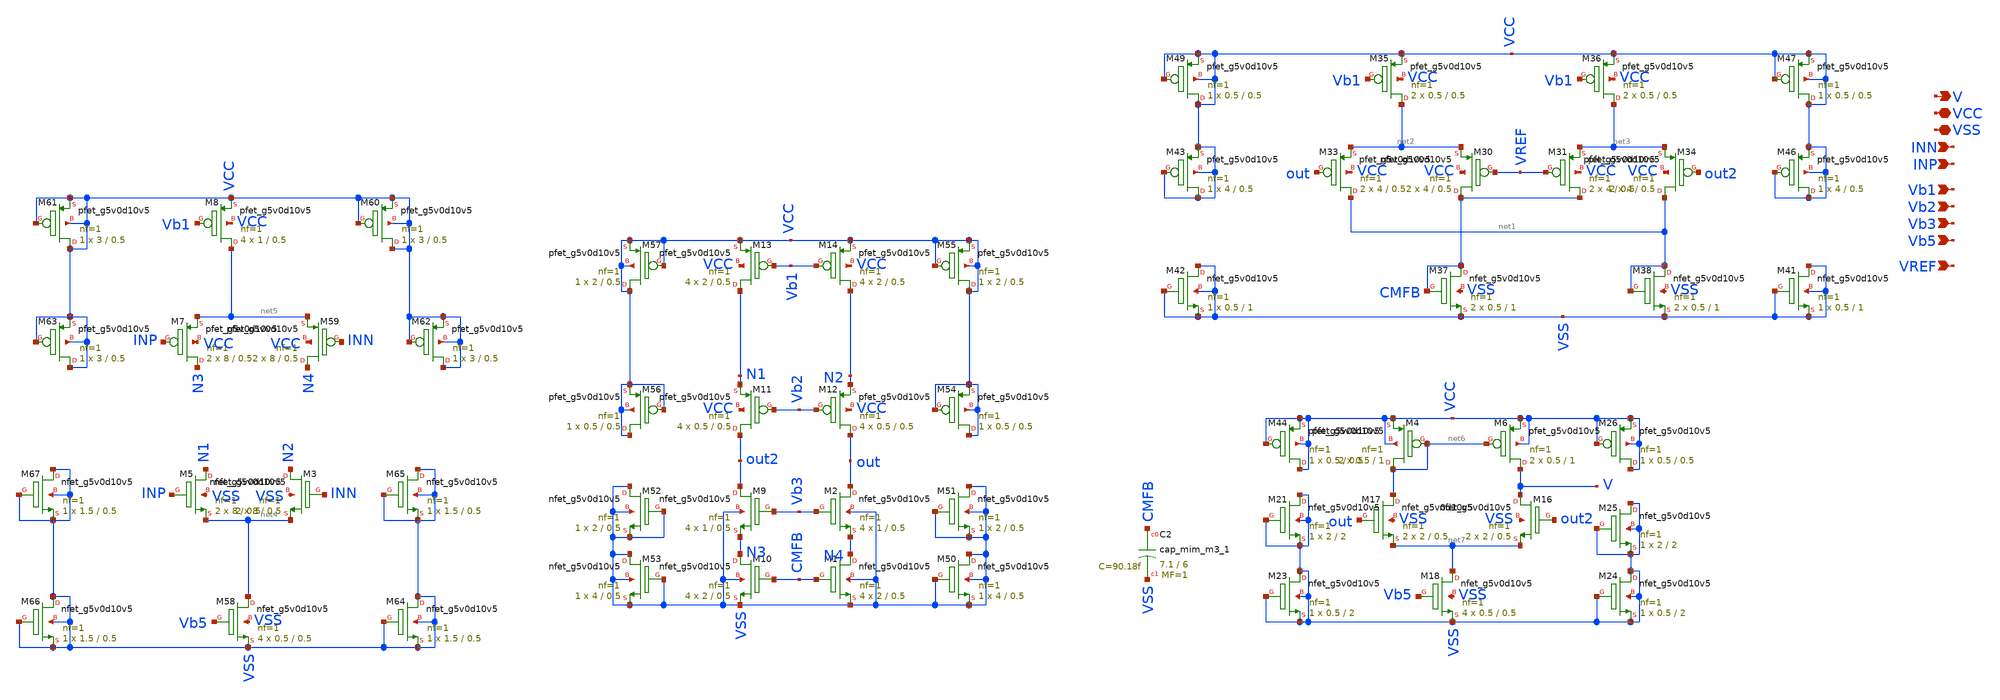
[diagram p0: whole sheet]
** sch_path: latest_working_comparator/total.sch
**.subckt total V VCC VSS INN INP Vb1 Vb2 Vb3 Vb5 VREF
*.opin V
*.iopin VCC
*.iopin VSS
*.ipin INN
*.ipin INP
*.ipin Vb1
*.ipin Vb2
*.ipin Vb3
*.ipin Vb5
*.ipin VREF
XM1 N4 CMFB VSS VSS sky130_fd_pr__nfet_g5v0d10v5 L=0.5 W=2 nf=1 ad='int((nf+1)/2) * W/nf * 0.29' as='int((nf+2)/2) * W/nf * 0.29'
+ pd='2*int((nf+1)/2) * (W/nf + 0.29)' ps='2*int((nf+2)/2) * (W/nf + 0.29)' nrd='0.29 / W' nrs='0.29 / W'
+ sa=0 sb=0 sd=0 mult=4 m=4
XM2 out Vb3 N4 VSS sky130_fd_pr__nfet_g5v0d10v5 L=0.5 W=1 nf=1 ad='int((nf+1)/2) * W/nf * 0.29' as='int((nf+2)/2) * W/nf * 0.29'
+ pd='2*int((nf+1)/2) * (W/nf + 0.29)' ps='2*int((nf+2)/2) * (W/nf + 0.29)' nrd='0.29 / W' nrs='0.29 / W'
+ sa=0 sb=0 sd=0 mult=4 m=4
XM9 out2 Vb3 N3 VSS sky130_fd_pr__nfet_g5v0d10v5 L=0.5 W=1 nf=1 ad='int((nf+1)/2) * W/nf * 0.29' as='int((nf+2)/2) * W/nf * 0.29'
+ pd='2*int((nf+1)/2) * (W/nf + 0.29)' ps='2*int((nf+2)/2) * (W/nf + 0.29)' nrd='0.29 / W' nrs='0.29 / W'
+ sa=0 sb=0 sd=0 mult=4 m=4
XM10 N3 CMFB VSS VSS sky130_fd_pr__nfet_g5v0d10v5 L=0.5 W=2 nf=1 ad='int((nf+1)/2) * W/nf * 0.29' as='int((nf+2)/2) * W/nf * 0.29'
+ pd='2*int((nf+1)/2) * (W/nf + 0.29)' ps='2*int((nf+2)/2) * (W/nf + 0.29)' nrd='0.29 / W' nrs='0.29 / W'
+ sa=0 sb=0 sd=0 mult=4 m=4
XM11 out2 Vb2 N1 VCC sky130_fd_pr__pfet_g5v0d10v5 L=0.5 W=0.5 nf=1 ad='int((nf+1)/2) * W/nf * 0.29' as='int((nf+2)/2) * W/nf * 0.29'
+ pd='2*int((nf+1)/2) * (W/nf + 0.29)' ps='2*int((nf+2)/2) * (W/nf + 0.29)' nrd='0.29 / W' nrs='0.29 / W'
+ sa=0 sb=0 sd=0 mult=4 m=4
XM12 out Vb2 N2 VCC sky130_fd_pr__pfet_g5v0d10v5 L=0.5 W=0.5 nf=1 ad='int((nf+1)/2) * W/nf * 0.29' as='int((nf+2)/2) * W/nf * 0.29'
+ pd='2*int((nf+1)/2) * (W/nf + 0.29)' ps='2*int((nf+2)/2) * (W/nf + 0.29)' nrd='0.29 / W' nrs='0.29 / W'
+ sa=0 sb=0 sd=0 mult=4 m=4
XM13 N1 Vb1 VCC VCC sky130_fd_pr__pfet_g5v0d10v5 L=0.5 W=2 nf=1 ad='int((nf+1)/2) * W/nf * 0.29' as='int((nf+2)/2) * W/nf * 0.29'
+ pd='2*int((nf+1)/2) * (W/nf + 0.29)' ps='2*int((nf+2)/2) * (W/nf + 0.29)' nrd='0.29 / W' nrs='0.29 / W'
+ sa=0 sb=0 sd=0 mult=4 m=4
XM14 N2 Vb1 VCC VCC sky130_fd_pr__pfet_g5v0d10v5 L=0.5 W=2 nf=1 ad='int((nf+1)/2) * W/nf * 0.29' as='int((nf+2)/2) * W/nf * 0.29'
+ pd='2*int((nf+1)/2) * (W/nf + 0.29)' ps='2*int((nf+2)/2) * (W/nf + 0.29)' nrd='0.29 / W' nrs='0.29 / W'
+ sa=0 sb=0 sd=0 mult=4 m=4
XM30 CMFB VREF net2 VCC sky130_fd_pr__pfet_g5v0d10v5 L=0.5 W=4 nf=1 ad='int((nf+1)/2) * W/nf * 0.29'
+ as='int((nf+2)/2) * W/nf * 0.29' pd='2*int((nf+1)/2) * (W/nf + 0.29)' ps='2*int((nf+2)/2) * (W/nf + 0.29)'
+ nrd='0.29 / W' nrs='0.29 / W' sa=0 sb=0 sd=0 mult=2 m=2
XM31 CMFB VREF net3 VCC sky130_fd_pr__pfet_g5v0d10v5 L=0.5 W=4 nf=1 ad='int((nf+1)/2) * W/nf * 0.29'
+ as='int((nf+2)/2) * W/nf * 0.29' pd='2*int((nf+1)/2) * (W/nf + 0.29)' ps='2*int((nf+2)/2) * (W/nf + 0.29)'
+ nrd='0.29 / W' nrs='0.29 / W' sa=0 sb=0 sd=0 mult=2 m=2
XM33 net1 out net2 VCC sky130_fd_pr__pfet_g5v0d10v5 L=0.5 W=4 nf=1 ad='int((nf+1)/2) * W/nf * 0.29' as='int((nf+2)/2) * W/nf * 0.29'
+ pd='2*int((nf+1)/2) * (W/nf + 0.29)' ps='2*int((nf+2)/2) * (W/nf + 0.29)' nrd='0.29 / W' nrs='0.29 / W'
+ sa=0 sb=0 sd=0 mult=2 m=2
XM34 net1 out2 net3 VCC sky130_fd_pr__pfet_g5v0d10v5 L=0.5 W=4 nf=1 ad='int((nf+1)/2) * W/nf * 0.29'
+ as='int((nf+2)/2) * W/nf * 0.29' pd='2*int((nf+1)/2) * (W/nf + 0.29)' ps='2*int((nf+2)/2) * (W/nf + 0.29)'
+ nrd='0.29 / W' nrs='0.29 / W' sa=0 sb=0 sd=0 mult=2 m=2
XM35 net2 Vb1 VCC VCC sky130_fd_pr__pfet_g5v0d10v5 L=0.5 W=0.5 nf=1 ad='int((nf+1)/2) * W/nf * 0.29'
+ as='int((nf+2)/2) * W/nf * 0.29' pd='2*int((nf+1)/2) * (W/nf + 0.29)' ps='2*int((nf+2)/2) * (W/nf + 0.29)'
+ nrd='0.29 / W' nrs='0.29 / W' sa=0 sb=0 sd=0 mult=2 m=2
XM36 net3 Vb1 VCC VCC sky130_fd_pr__pfet_g5v0d10v5 L=0.5 W=0.5 nf=1 ad='int((nf+1)/2) * W/nf * 0.29'
+ as='int((nf+2)/2) * W/nf * 0.29' pd='2*int((nf+1)/2) * (W/nf + 0.29)' ps='2*int((nf+2)/2) * (W/nf + 0.29)'
+ nrd='0.29 / W' nrs='0.29 / W' sa=0 sb=0 sd=0 mult=2 m=2
XM37 CMFB CMFB VSS VSS sky130_fd_pr__nfet_g5v0d10v5 L=1 W=0.5 nf=1 ad='int((nf+1)/2) * W/nf * 0.29' as='int((nf+2)/2) * W/nf * 0.29'
+ pd='2*int((nf+1)/2) * (W/nf + 0.29)' ps='2*int((nf+2)/2) * (W/nf + 0.29)' nrd='0.29 / W' nrs='0.29 / W'
+ sa=0 sb=0 sd=0 mult=2 m=2
XM38 net1 net1 VSS VSS sky130_fd_pr__nfet_g5v0d10v5 L=1 W=0.5 nf=1 ad='int((nf+1)/2) * W/nf * 0.29' as='int((nf+2)/2) * W/nf * 0.29'
+ pd='2*int((nf+1)/2) * (W/nf + 0.29)' ps='2*int((nf+2)/2) * (W/nf + 0.29)' nrd='0.29 / W' nrs='0.29 / W'
+ sa=0 sb=0 sd=0 mult=2 m=2
XM41 VSS VSS VSS VSS sky130_fd_pr__nfet_g5v0d10v5 L=1 W=0.5 nf=1 ad='int((nf+1)/2) * W/nf * 0.29' as='int((nf+2)/2) * W/nf * 0.29'
+ pd='2*int((nf+1)/2) * (W/nf + 0.29)' ps='2*int((nf+2)/2) * (W/nf + 0.29)' nrd='0.29 / W' nrs='0.29 / W'
+ sa=0 sb=0 sd=0 mult=1 m=1
XM42 VSS VSS VSS VSS sky130_fd_pr__nfet_g5v0d10v5 L=1 W=0.5 nf=1 ad='int((nf+1)/2) * W/nf * 0.29' as='int((nf+2)/2) * W/nf * 0.29'
+ pd='2*int((nf+1)/2) * (W/nf + 0.29)' ps='2*int((nf+2)/2) * (W/nf + 0.29)' nrd='0.29 / W' nrs='0.29 / W'
+ sa=0 sb=0 sd=0 mult=1 m=1
XM43 VCC VCC VCC VCC sky130_fd_pr__pfet_g5v0d10v5 L=0.5 W=4 nf=1 ad='int((nf+1)/2) * W/nf * 0.29' as='int((nf+2)/2) * W/nf * 0.29'
+ pd='2*int((nf+1)/2) * (W/nf + 0.29)' ps='2*int((nf+2)/2) * (W/nf + 0.29)' nrd='0.29 / W' nrs='0.29 / W'
+ sa=0 sb=0 sd=0 mult=1 m=1
XM47 VCC VCC VCC VCC sky130_fd_pr__pfet_g5v0d10v5 L=0.5 W=0.5 nf=1 ad='int((nf+1)/2) * W/nf * 0.29' as='int((nf+2)/2) * W/nf * 0.29'
+ pd='2*int((nf+1)/2) * (W/nf + 0.29)' ps='2*int((nf+2)/2) * (W/nf + 0.29)' nrd='0.29 / W' nrs='0.29 / W'
+ sa=0 sb=0 sd=0 mult=1 m=1
XM49 VCC VCC VCC VCC sky130_fd_pr__pfet_g5v0d10v5 L=0.5 W=0.5 nf=1 ad='int((nf+1)/2) * W/nf * 0.29' as='int((nf+2)/2) * W/nf * 0.29'
+ pd='2*int((nf+1)/2) * (W/nf + 0.29)' ps='2*int((nf+2)/2) * (W/nf + 0.29)' nrd='0.29 / W' nrs='0.29 / W'
+ sa=0 sb=0 sd=0 mult=1 m=1
XM46 VCC VCC VCC VCC sky130_fd_pr__pfet_g5v0d10v5 L=0.5 W=4 nf=1 ad='int((nf+1)/2) * W/nf * 0.29' as='int((nf+2)/2) * W/nf * 0.29'
+ pd='2*int((nf+1)/2) * (W/nf + 0.29)' ps='2*int((nf+2)/2) * (W/nf + 0.29)' nrd='0.29 / W' nrs='0.29 / W'
+ sa=0 sb=0 sd=0 mult=1 m=1
XM50 VSS VSS VSS VSS sky130_fd_pr__nfet_g5v0d10v5 L=0.5 W=4 nf=1 ad='int((nf+1)/2) * W/nf * 0.29' as='int((nf+2)/2) * W/nf * 0.29'
+ pd='2*int((nf+1)/2) * (W/nf + 0.29)' ps='2*int((nf+2)/2) * (W/nf + 0.29)' nrd='0.29 / W' nrs='0.29 / W'
+ sa=0 sb=0 sd=0 mult=1 m=1
XM51 VSS VSS VSS VSS sky130_fd_pr__nfet_g5v0d10v5 L=0.5 W=2 nf=1 ad='int((nf+1)/2) * W/nf * 0.29' as='int((nf+2)/2) * W/nf * 0.29'
+ pd='2*int((nf+1)/2) * (W/nf + 0.29)' ps='2*int((nf+2)/2) * (W/nf + 0.29)' nrd='0.29 / W' nrs='0.29 / W'
+ sa=0 sb=0 sd=0 mult=1 m=1
XM52 VSS VSS VSS VSS sky130_fd_pr__nfet_g5v0d10v5 L=0.5 W=2 nf=1 ad='int((nf+1)/2) * W/nf * 0.29' as='int((nf+2)/2) * W/nf * 0.29'
+ pd='2*int((nf+1)/2) * (W/nf + 0.29)' ps='2*int((nf+2)/2) * (W/nf + 0.29)' nrd='0.29 / W' nrs='0.29 / W'
+ sa=0 sb=0 sd=0 mult=1 m=1
XM53 VSS VSS VSS VSS sky130_fd_pr__nfet_g5v0d10v5 L=0.5 W=4 nf=1 ad='int((nf+1)/2) * W/nf * 0.29' as='int((nf+2)/2) * W/nf * 0.29'
+ pd='2*int((nf+1)/2) * (W/nf + 0.29)' ps='2*int((nf+2)/2) * (W/nf + 0.29)' nrd='0.29 / W' nrs='0.29 / W'
+ sa=0 sb=0 sd=0 mult=1 m=1
XM54 VCC VCC VCC VCC sky130_fd_pr__pfet_g5v0d10v5 L=0.5 W=0.5 nf=1 ad='int((nf+1)/2) * W/nf * 0.29' as='int((nf+2)/2) * W/nf * 0.29'
+ pd='2*int((nf+1)/2) * (W/nf + 0.29)' ps='2*int((nf+2)/2) * (W/nf + 0.29)' nrd='0.29 / W' nrs='0.29 / W'
+ sa=0 sb=0 sd=0 mult=1 m=1
XM55 VCC VCC VCC VCC sky130_fd_pr__pfet_g5v0d10v5 L=0.5 W=2 nf=1 ad='int((nf+1)/2) * W/nf * 0.29' as='int((nf+2)/2) * W/nf * 0.29'
+ pd='2*int((nf+1)/2) * (W/nf + 0.29)' ps='2*int((nf+2)/2) * (W/nf + 0.29)' nrd='0.29 / W' nrs='0.29 / W'
+ sa=0 sb=0 sd=0 mult=1 m=1
XM56 VCC VCC VCC VCC sky130_fd_pr__pfet_g5v0d10v5 L=0.5 W=0.5 nf=1 ad='int((nf+1)/2) * W/nf * 0.29' as='int((nf+2)/2) * W/nf * 0.29'
+ pd='2*int((nf+1)/2) * (W/nf + 0.29)' ps='2*int((nf+2)/2) * (W/nf + 0.29)' nrd='0.29 / W' nrs='0.29 / W'
+ sa=0 sb=0 sd=0 mult=1 m=1
XM57 VCC VCC VCC VCC sky130_fd_pr__pfet_g5v0d10v5 L=0.5 W=2 nf=1 ad='int((nf+1)/2) * W/nf * 0.29' as='int((nf+2)/2) * W/nf * 0.29'
+ pd='2*int((nf+1)/2) * (W/nf + 0.29)' ps='2*int((nf+2)/2) * (W/nf + 0.29)' nrd='0.29 / W' nrs='0.29 / W'
+ sa=0 sb=0 sd=0 mult=1 m=1
XC2 CMFB VSS sky130_fd_pr__cap_mim_m3_1 W=7.1 L=6 MF=1 m=1
XM3 N2 INN net4 VSS sky130_fd_pr__nfet_g5v0d10v5 L=0.5 W=8 nf=1 ad='int((nf+1)/2) * W/nf * 0.29' as='int((nf+2)/2) * W/nf * 0.29'
+ pd='2*int((nf+1)/2) * (W/nf + 0.29)' ps='2*int((nf+2)/2) * (W/nf + 0.29)' nrd='0.29 / W' nrs='0.29 / W'
+ sa=0 sb=0 sd=0 mult=2 m=2
XM5 N1 INP net4 VSS sky130_fd_pr__nfet_g5v0d10v5 L=0.5 W=8 nf=1 ad='int((nf+1)/2) * W/nf * 0.29' as='int((nf+2)/2) * W/nf * 0.29'
+ pd='2*int((nf+1)/2) * (W/nf + 0.29)' ps='2*int((nf+2)/2) * (W/nf + 0.29)' nrd='0.29 / W' nrs='0.29 / W'
+ sa=0 sb=0 sd=0 mult=2 m=2
XM7 N3 INP net5 VCC sky130_fd_pr__pfet_g5v0d10v5 L=0.5 W=8 nf=1 ad='int((nf+1)/2) * W/nf * 0.29' as='int((nf+2)/2) * W/nf * 0.29'
+ pd='2*int((nf+1)/2) * (W/nf + 0.29)' ps='2*int((nf+2)/2) * (W/nf + 0.29)' nrd='0.29 / W' nrs='0.29 / W'
+ sa=0 sb=0 sd=0 mult=2 m=2
XM8 net5 Vb1 VCC VCC sky130_fd_pr__pfet_g5v0d10v5 L=0.5 W=1 nf=1 ad='int((nf+1)/2) * W/nf * 0.29' as='int((nf+2)/2) * W/nf * 0.29'
+ pd='2*int((nf+1)/2) * (W/nf + 0.29)' ps='2*int((nf+2)/2) * (W/nf + 0.29)' nrd='0.29 / W' nrs='0.29 / W'
+ sa=0 sb=0 sd=0 mult=4 m=4
XM58 net4 Vb5 VSS VSS sky130_fd_pr__nfet_g5v0d10v5 L=0.5 W=0.5 nf=1 ad='int((nf+1)/2) * W/nf * 0.29'
+ as='int((nf+2)/2) * W/nf * 0.29' pd='2*int((nf+1)/2) * (W/nf + 0.29)' ps='2*int((nf+2)/2) * (W/nf + 0.29)'
+ nrd='0.29 / W' nrs='0.29 / W' sa=0 sb=0 sd=0 mult=4 m=4
XM59 N4 INN net5 VCC sky130_fd_pr__pfet_g5v0d10v5 L=0.5 W=8 nf=1 ad='int((nf+1)/2) * W/nf * 0.29' as='int((nf+2)/2) * W/nf * 0.29'
+ pd='2*int((nf+1)/2) * (W/nf + 0.29)' ps='2*int((nf+2)/2) * (W/nf + 0.29)' nrd='0.29 / W' nrs='0.29 / W'
+ sa=0 sb=0 sd=0 mult=2 m=2
XM60 VCC VCC VCC VCC sky130_fd_pr__pfet_g5v0d10v5 L=0.5 W=3 nf=1 ad='int((nf+1)/2) * W/nf * 0.29' as='int((nf+2)/2) * W/nf * 0.29'
+ pd='2*int((nf+1)/2) * (W/nf + 0.29)' ps='2*int((nf+2)/2) * (W/nf + 0.29)' nrd='0.29 / W' nrs='0.29 / W'
+ sa=0 sb=0 sd=0 mult=1 m=1
XM61 VCC VCC VCC VCC sky130_fd_pr__pfet_g5v0d10v5 L=0.5 W=3 nf=1 ad='int((nf+1)/2) * W/nf * 0.29' as='int((nf+2)/2) * W/nf * 0.29'
+ pd='2*int((nf+1)/2) * (W/nf + 0.29)' ps='2*int((nf+2)/2) * (W/nf + 0.29)' nrd='0.29 / W' nrs='0.29 / W'
+ sa=0 sb=0 sd=0 mult=1 m=1
XM62 VCC VCC VCC VCC sky130_fd_pr__pfet_g5v0d10v5 L=0.5 W=3 nf=1 ad='int((nf+1)/2) * W/nf * 0.29' as='int((nf+2)/2) * W/nf * 0.29'
+ pd='2*int((nf+1)/2) * (W/nf + 0.29)' ps='2*int((nf+2)/2) * (W/nf + 0.29)' nrd='0.29 / W' nrs='0.29 / W'
+ sa=0 sb=0 sd=0 mult=1 m=1
XM63 VCC VCC VCC VCC sky130_fd_pr__pfet_g5v0d10v5 L=0.5 W=3 nf=1 ad='int((nf+1)/2) * W/nf * 0.29' as='int((nf+2)/2) * W/nf * 0.29'
+ pd='2*int((nf+1)/2) * (W/nf + 0.29)' ps='2*int((nf+2)/2) * (W/nf + 0.29)' nrd='0.29 / W' nrs='0.29 / W'
+ sa=0 sb=0 sd=0 mult=1 m=1
XM64 VSS VSS VSS VSS sky130_fd_pr__nfet_g5v0d10v5 L=0.5 W=1.5 nf=1 ad='int((nf+1)/2) * W/nf * 0.29' as='int((nf+2)/2) * W/nf * 0.29'
+ pd='2*int((nf+1)/2) * (W/nf + 0.29)' ps='2*int((nf+2)/2) * (W/nf + 0.29)' nrd='0.29 / W' nrs='0.29 / W'
+ sa=0 sb=0 sd=0 mult=1 m=1
XM65 VSS VSS VSS VSS sky130_fd_pr__nfet_g5v0d10v5 L=0.5 W=1.5 nf=1 ad='int((nf+1)/2) * W/nf * 0.29' as='int((nf+2)/2) * W/nf * 0.29'
+ pd='2*int((nf+1)/2) * (W/nf + 0.29)' ps='2*int((nf+2)/2) * (W/nf + 0.29)' nrd='0.29 / W' nrs='0.29 / W'
+ sa=0 sb=0 sd=0 mult=1 m=1
XM66 VSS VSS VSS VSS sky130_fd_pr__nfet_g5v0d10v5 L=0.5 W=1.5 nf=1 ad='int((nf+1)/2) * W/nf * 0.29' as='int((nf+2)/2) * W/nf * 0.29'
+ pd='2*int((nf+1)/2) * (W/nf + 0.29)' ps='2*int((nf+2)/2) * (W/nf + 0.29)' nrd='0.29 / W' nrs='0.29 / W'
+ sa=0 sb=0 sd=0 mult=1 m=1
XM67 VSS VSS VSS VSS sky130_fd_pr__nfet_g5v0d10v5 L=0.5 W=1.5 nf=1 ad='int((nf+1)/2) * W/nf * 0.29' as='int((nf+2)/2) * W/nf * 0.29'
+ pd='2*int((nf+1)/2) * (W/nf + 0.29)' ps='2*int((nf+2)/2) * (W/nf + 0.29)' nrd='0.29 / W' nrs='0.29 / W'
+ sa=0 sb=0 sd=0 mult=1 m=1
XM4 net6 net6 VCC VCC sky130_fd_pr__pfet_g5v0d10v5 L=1 W=0.5 nf=1 ad='int((nf+1)/2) * W/nf * 0.29' as='int((nf+2)/2) * W/nf * 0.29'
+ pd='2*int((nf+1)/2) * (W/nf + 0.29)' ps='2*int((nf+2)/2) * (W/nf + 0.29)' nrd='0.29 / W' nrs='0.29 / W'
+ sa=0 sb=0 sd=0 mult=2 m=2
XM6 V net6 VCC VCC sky130_fd_pr__pfet_g5v0d10v5 L=1 W=0.5 nf=1 ad='int((nf+1)/2) * W/nf * 0.29' as='int((nf+2)/2) * W/nf * 0.29'
+ pd='2*int((nf+1)/2) * (W/nf + 0.29)' ps='2*int((nf+2)/2) * (W/nf + 0.29)' nrd='0.29 / W' nrs='0.29 / W'
+ sa=0 sb=0 sd=0 mult=2 m=2
XM16 V out2 net7 VSS sky130_fd_pr__nfet_g5v0d10v5 L=0.5 W=2 nf=1 ad='int((nf+1)/2) * W/nf * 0.29' as='int((nf+2)/2) * W/nf * 0.29'
+ pd='2*int((nf+1)/2) * (W/nf + 0.29)' ps='2*int((nf+2)/2) * (W/nf + 0.29)' nrd='0.29 / W' nrs='0.29 / W'
+ sa=0 sb=0 sd=0 mult=2 m=2
XM17 net6 out net7 VSS sky130_fd_pr__nfet_g5v0d10v5 L=0.5 W=2 nf=1 ad='int((nf+1)/2) * W/nf * 0.29' as='int((nf+2)/2) * W/nf * 0.29'
+ pd='2*int((nf+1)/2) * (W/nf + 0.29)' ps='2*int((nf+2)/2) * (W/nf + 0.29)' nrd='0.29 / W' nrs='0.29 / W'
+ sa=0 sb=0 sd=0 mult=2 m=2
XM18 net7 Vb5 VSS VSS sky130_fd_pr__nfet_g5v0d10v5 L=0.5 W=0.5 nf=1 ad='int((nf+1)/2) * W/nf * 0.29'
+ as='int((nf+2)/2) * W/nf * 0.29' pd='2*int((nf+1)/2) * (W/nf + 0.29)' ps='2*int((nf+2)/2) * (W/nf + 0.29)'
+ nrd='0.29 / W' nrs='0.29 / W' sa=0 sb=0 sd=0 mult=4 m=4
XM21 VSS VSS VSS VSS sky130_fd_pr__nfet_g5v0d10v5 L=2 W=2 nf=1 ad='int((nf+1)/2) * W/nf * 0.29' as='int((nf+2)/2) * W/nf * 0.29'
+ pd='2*int((nf+1)/2) * (W/nf + 0.29)' ps='2*int((nf+2)/2) * (W/nf + 0.29)' nrd='0.29 / W' nrs='0.29 / W'
+ sa=0 sb=0 sd=0 mult=1 m=1
XM23 VSS VSS VSS VSS sky130_fd_pr__nfet_g5v0d10v5 L=2 W=0.5 nf=1 ad='int((nf+1)/2) * W/nf * 0.29' as='int((nf+2)/2) * W/nf * 0.29'
+ pd='2*int((nf+1)/2) * (W/nf + 0.29)' ps='2*int((nf+2)/2) * (W/nf + 0.29)' nrd='0.29 / W' nrs='0.29 / W'
+ sa=0 sb=0 sd=0 mult=1 m=1
XM24 VSS VSS VSS VSS sky130_fd_pr__nfet_g5v0d10v5 L=2 W=0.5 nf=1 ad='int((nf+1)/2) * W/nf * 0.29' as='int((nf+2)/2) * W/nf * 0.29'
+ pd='2*int((nf+1)/2) * (W/nf + 0.29)' ps='2*int((nf+2)/2) * (W/nf + 0.29)' nrd='0.29 / W' nrs='0.29 / W'
+ sa=0 sb=0 sd=0 mult=1 m=1
XM25 VSS VSS VSS VSS sky130_fd_pr__nfet_g5v0d10v5 L=2 W=2 nf=1 ad='int((nf+1)/2) * W/nf * 0.29' as='int((nf+2)/2) * W/nf * 0.29'
+ pd='2*int((nf+1)/2) * (W/nf + 0.29)' ps='2*int((nf+2)/2) * (W/nf + 0.29)' nrd='0.29 / W' nrs='0.29 / W'
+ sa=0 sb=0 sd=0 mult=1 m=1
XM26 VCC VCC VCC VCC sky130_fd_pr__pfet_g5v0d10v5 L=0.5 W=0.5 nf=1 ad='int((nf+1)/2) * W/nf * 0.29' as='int((nf+2)/2) * W/nf * 0.29'
+ pd='2*int((nf+1)/2) * (W/nf + 0.29)' ps='2*int((nf+2)/2) * (W/nf + 0.29)' nrd='0.29 / W' nrs='0.29 / W'
+ sa=0 sb=0 sd=0 mult=1 m=1
XM44 VCC VCC VCC VCC sky130_fd_pr__pfet_g5v0d10v5 L=0.5 W=0.5 nf=1 ad='int((nf+1)/2) * W/nf * 0.29' as='int((nf+2)/2) * W/nf * 0.29'
+ pd='2*int((nf+1)/2) * (W/nf + 0.29)' ps='2*int((nf+2)/2) * (W/nf + 0.29)' nrd='0.29 / W' nrs='0.29 / W'
+ sa=0 sb=0 sd=0 mult=1 m=1
**.ends
.end
